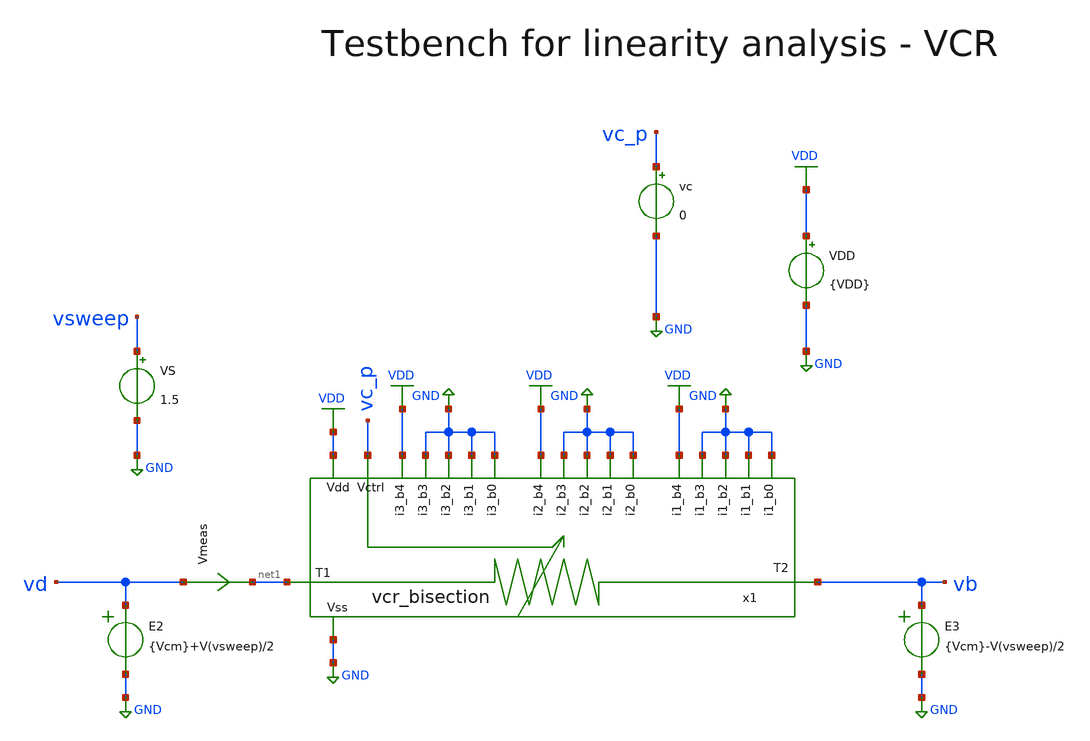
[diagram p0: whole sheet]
** sch_path: macros/heichips26_vcr/macros/vcr_bisection/testbenches/xschem/res_tb_linearity.sch
**.subckt res_tb_linearity
VDD VDD GND {VDD}
VS vsweep GND 1.5
Vmeas vd net1 0
.save i(vmeas)
E2 vd GND VOL=' {Vcm}+V(vsweep)/2 '
E3 vb GND VOL=' {Vcm}-V(vsweep)/2 '
vc vc_p GND 0
x1 GND GND VDD GND GND GND GND VDD GND GND GND GND VDD GND GND vc_p VDD GND vb net1 vcr_bisection
**** begin user architecture code

.lib cornerMOShv.lib mos_tt
.lib cornerRES.lib res_typ
.lib cornerDIO.lib dio_tt
.lib cornerCAP.lib cap_typ



* .include ../../../netlist/pex/inverter_magic_pex_3.spice
.param VDD=3.3
.csparam VDD=VDD
.param Vcm=0.8
.csparam Vcm=Vcm
.param temp=27
.options savecurrents klu method=gear reltol=1e-3 abstol=1e-15 gmin=1e-15 rshunt=1e13
.control
let vcc = 1.2

save all
set appendwrite



repeat 5
  alter vc $&vcc

  * DC Sweep
  dc VS -0.8 0.8 1m
  remzerovec
  let vcc = vcc + 0.5
end
write @schname\.raw
set appendwrite

* Plotting
plot dc1.v(vsweep)/(dc1.i(vmeas)) dc2.v(vsweep)/(dc2.i(vmeas)) dc3.v(vsweep)/(dc3.i(vmeas))
+ dc4.v(vsweep)/(dc4.i(vmeas)) dc5.v(vsweep)/(dc5.i(vmeas)) ylimit 0 50k

plot dc1.i(vmeas) dc2.i(vmeas) dc3.i(vmeas) dc4.i(vmeas) dc5.i(vmeas)

* Write Data
unset appendwrite
set wr_vecnames
set wr_singlescale
wrdata ../plot_simulations/data/@schname\.txt v(vc_p) dc1.v(vsweep)/(dc1.i(Vmeas))
+ dc2.v(vsweep)/(dc2.i(Vmeas)) dc3.v(vsweep)/(dc3.i(Vmeas)) dc4.v(vsweep)/(dc4.i(Vmeas)) dc5.v(vsweep)/(dc5.i(Vmeas))

write res_tb_linearity.raw

*quit
.endc


**** end user architecture code
**.ends
.GLOBAL GND
.GLOBAL VDD
.end
